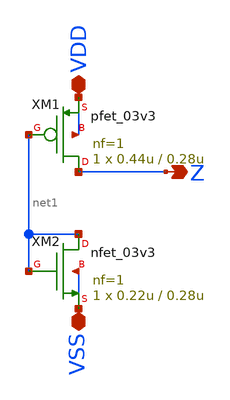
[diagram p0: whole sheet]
** sch_path: xschem_sn2/TIEH.sch
**.subckt TIEH VSS VDD Z
*.iopin VSS
*.iopin VDD
*.opin Z
XM1 Z net1 VDD VDD pfet_03v3 L=0.28u W=0.44u nf=1 ad='int((nf+1)/2) * W/nf * 0.18u' as='int((nf+2)/2) * W/nf * 0.18u'
+ pd='2*int((nf+1)/2) * (W/nf + 0.18u)' ps='2*int((nf+2)/2) * (W/nf + 0.18u)' nrd='0.18u / W' nrs='0.18u / W'
+ sa=0 sb=0 sd=0 m=1 par=1
XM2 net1 net1 VSS VSS nfet_03v3 L=0.28u W=0.22u nf=1 ad='int((nf+1)/2) * W/nf * 0.18u' as='int((nf+2)/2) * W/nf * 0.18u'
+ pd='2*int((nf+1)/2) * (W/nf + 0.18u)' ps='2*int((nf+2)/2) * (W/nf + 0.18u)' nrd='0.18u / W' nrs='0.18u / W'
+ sa=0 sb=0 sd=0 m=1 par=1
**.ends
.end
